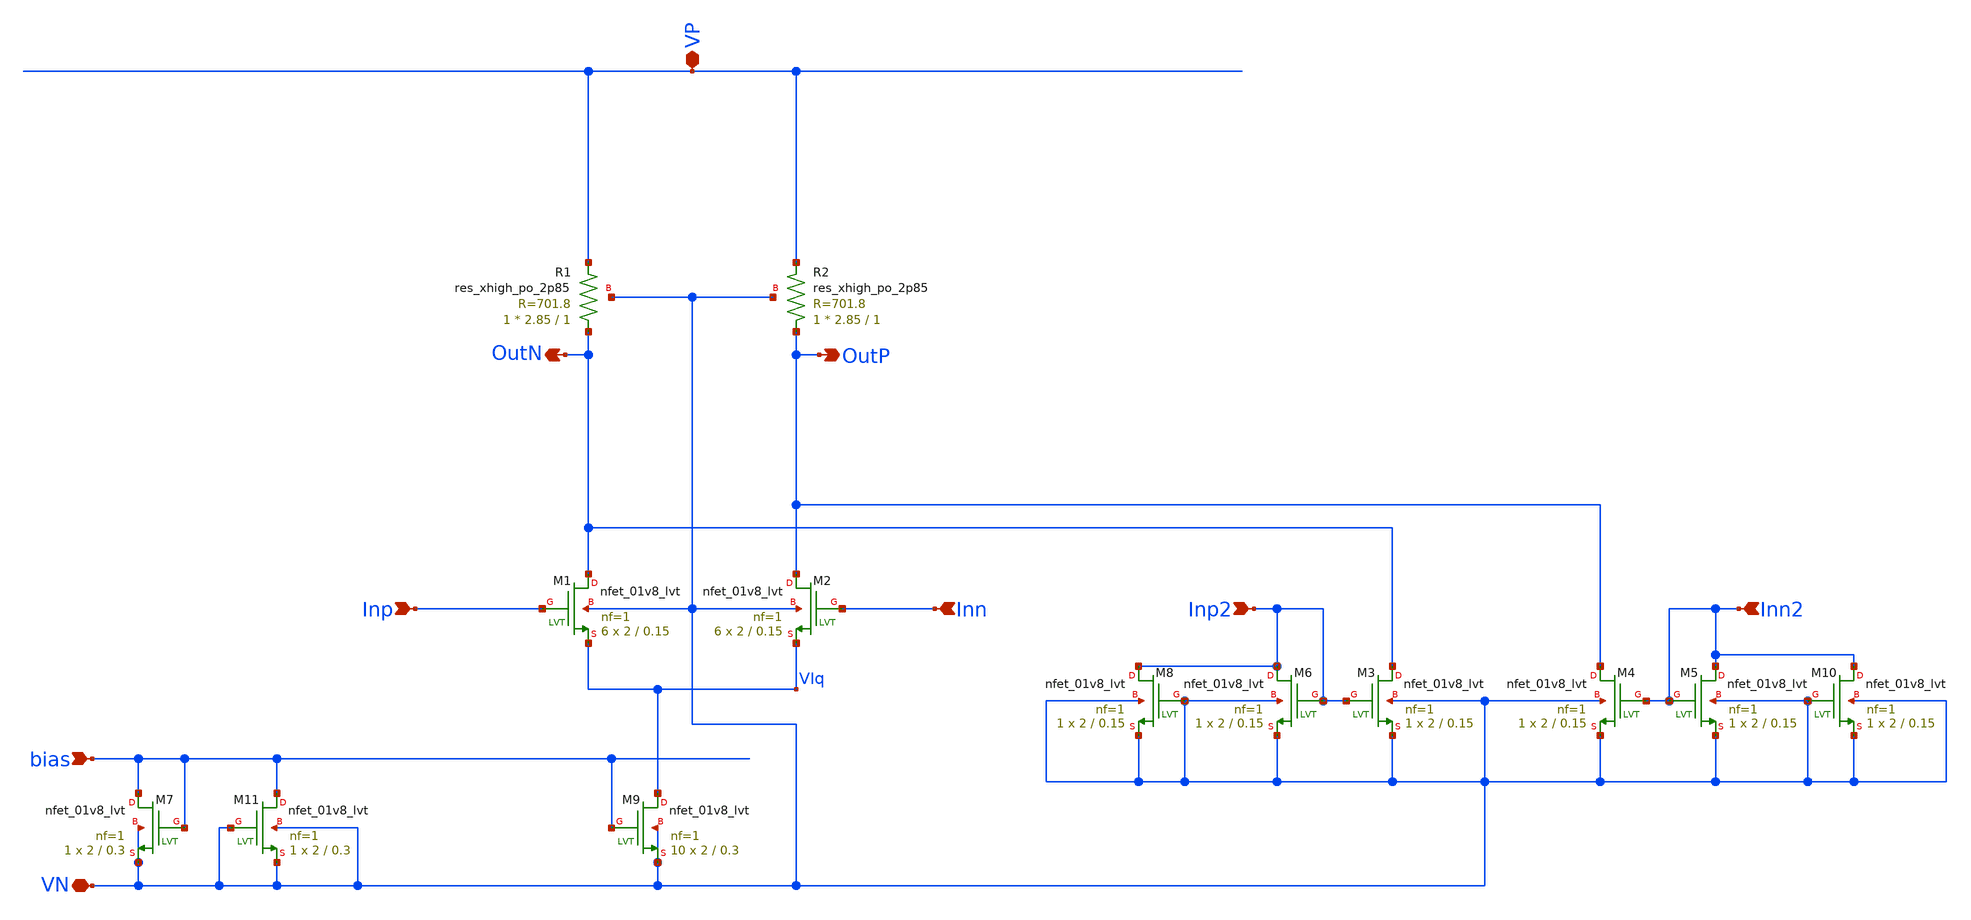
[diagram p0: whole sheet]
** sch_path: xschem/comp/comp_adv3_di.sch
**.subckt comp_adv3_di Inp bias Inn VP VN OutN OutP Inn2 Inp2
*.ipin Inp
*.ipin bias
*.ipin Inn
*.iopin VP
*.iopin VN
*.opin OutN
*.opin OutP
*.ipin Inn2
*.ipin Inp2
XM1 OutN Inp VIq VN sky130_fd_pr__nfet_01v8_lvt L=0.15 W=2 nf=1 ad='int((nf+1)/2) * W/nf * 0.29' as='int((nf+2)/2) * W/nf * 0.29'
+ pd='2*int((nf+1)/2) * (W/nf + 0.29)' ps='2*int((nf+2)/2) * (W/nf + 0.29)' nrd='0.29 / W' nrs='0.29 / W'
+ sa=0 sb=0 sd=0 mult=6 m=6
XM2 OutP Inn VIq VN sky130_fd_pr__nfet_01v8_lvt L=0.15 W=2 nf=1 ad='int((nf+1)/2) * W/nf * 0.29' as='int((nf+2)/2) * W/nf * 0.29'
+ pd='2*int((nf+1)/2) * (W/nf + 0.29)' ps='2*int((nf+2)/2) * (W/nf + 0.29)' nrd='0.29 / W' nrs='0.29 / W'
+ sa=0 sb=0 sd=0 mult=6 m=6
XM7 bias bias VN VN sky130_fd_pr__nfet_01v8_lvt L=0.3 W=2 nf=1 ad='int((nf+1)/2) * W/nf * 0.29' as='int((nf+2)/2) * W/nf * 0.29'
+ pd='2*int((nf+1)/2) * (W/nf + 0.29)' ps='2*int((nf+2)/2) * (W/nf + 0.29)' nrd='0.29 / W' nrs='0.29 / W'
+ sa=0 sb=0 sd=0 mult=1 m=1
XM9 VIq bias VN VN sky130_fd_pr__nfet_01v8_lvt L=0.3 W=2 nf=1 ad='int((nf+1)/2) * W/nf * 0.29' as='int((nf+2)/2) * W/nf * 0.29'
+ pd='2*int((nf+1)/2) * (W/nf + 0.29)' ps='2*int((nf+2)/2) * (W/nf + 0.29)' nrd='0.29 / W' nrs='0.29 / W'
+ sa=0 sb=0 sd=0 mult=10 m=10
XR1 OutN VP VN sky130_fd_pr__res_xhigh_po_2p85 L=1 mult=1 m=1
XR2 OutP VP VN sky130_fd_pr__res_xhigh_po_2p85 L=1 mult=1 m=1
XM3 OutN Inp2 VN VN sky130_fd_pr__nfet_01v8_lvt L=0.15 W=2 nf=1 ad='int((nf+1)/2) * W/nf * 0.29' as='int((nf+2)/2) * W/nf * 0.29'
+ pd='2*int((nf+1)/2) * (W/nf + 0.29)' ps='2*int((nf+2)/2) * (W/nf + 0.29)' nrd='0.29 / W' nrs='0.29 / W'
+ sa=0 sb=0 sd=0 mult=1 m=1
XM4 OutP Inn2 VN VN sky130_fd_pr__nfet_01v8_lvt L=0.15 W=2 nf=1 ad='int((nf+1)/2) * W/nf * 0.29' as='int((nf+2)/2) * W/nf * 0.29'
+ pd='2*int((nf+1)/2) * (W/nf + 0.29)' ps='2*int((nf+2)/2) * (W/nf + 0.29)' nrd='0.29 / W' nrs='0.29 / W'
+ sa=0 sb=0 sd=0 mult=1 m=1
XM5 Inn2 Inn2 VN VN sky130_fd_pr__nfet_01v8_lvt L=0.15 W=2 nf=1 ad='int((nf+1)/2) * W/nf * 0.29' as='int((nf+2)/2) * W/nf * 0.29'
+ pd='2*int((nf+1)/2) * (W/nf + 0.29)' ps='2*int((nf+2)/2) * (W/nf + 0.29)' nrd='0.29 / W' nrs='0.29 / W'
+ sa=0 sb=0 sd=0 mult=1 m=1
XM6 Inp2 Inp2 VN VN sky130_fd_pr__nfet_01v8_lvt L=0.15 W=2 nf=1 ad='int((nf+1)/2) * W/nf * 0.29' as='int((nf+2)/2) * W/nf * 0.29'
+ pd='2*int((nf+1)/2) * (W/nf + 0.29)' ps='2*int((nf+2)/2) * (W/nf + 0.29)' nrd='0.29 / W' nrs='0.29 / W'
+ sa=0 sb=0 sd=0 mult=1 m=1
XM8 Inp2 VN VN VN sky130_fd_pr__nfet_01v8_lvt L=0.15 W=2 nf=1 ad='int((nf+1)/2) * W/nf * 0.29' as='int((nf+2)/2) * W/nf * 0.29'
+ pd='2*int((nf+1)/2) * (W/nf + 0.29)' ps='2*int((nf+2)/2) * (W/nf + 0.29)' nrd='0.29 / W' nrs='0.29 / W'
+ sa=0 sb=0 sd=0 mult=1 m=1
XM10 Inn2 VN VN VN sky130_fd_pr__nfet_01v8_lvt L=0.15 W=2 nf=1 ad='int((nf+1)/2) * W/nf * 0.29' as='int((nf+2)/2) * W/nf * 0.29'
+ pd='2*int((nf+1)/2) * (W/nf + 0.29)' ps='2*int((nf+2)/2) * (W/nf + 0.29)' nrd='0.29 / W' nrs='0.29 / W'
+ sa=0 sb=0 sd=0 mult=1 m=1
XM11 bias VN VN VN sky130_fd_pr__nfet_01v8_lvt L=0.3 W=2 nf=1 ad='int((nf+1)/2) * W/nf * 0.29' as='int((nf+2)/2) * W/nf * 0.29'
+ pd='2*int((nf+1)/2) * (W/nf + 0.29)' ps='2*int((nf+2)/2) * (W/nf + 0.29)' nrd='0.29 / W' nrs='0.29 / W'
+ sa=0 sb=0 sd=0 mult=1 m=1
**** begin user architecture code

*.lib $::SKYWATER_MODELS/sky130.lib.spice tt
.lib $::SKYWATER_MODELS/sky130.lib.spice.tt.red tt



*.options savecurrents
.option warn=1
.control
set wr_vecnames
set wr_singlescale
* Power consumption
op
* save all
* #OP#
print @m.xm1.msky130_fd_pr__nfet_01v8_lvt[gds]
print vdd#branch
print v(vm2d)
print v(vm3d)
print v(UD_M5)
wrdata 'result_op.csv' vdd#branch
ac dec 10 1 10G
meas ac dc_gain_vm2d FIND vdb(vm2d) AT=1
let bw_amp_vm2d=dc_gain_vm2d-3
meas ac dc_gain_vm3d FIND vdb(vm3d) AT=1
let bw_amp_vm3d=dc_gain_vm3d-3
meas ac bw_vm2d when vdb(vm2d)=bw_amp_vm2d
meas ac bw_vm3d when vdb(vm3d)=bw_amp_vm3d
*MEAS AC phasem FIND vp(vm2d) WHEN vdb(vm2d)=0
* wrdata 'result_ac.csv' dc_gain bw
* plot vdb(vm2D) log
*
*print WM3D
run
reset
save @m.xm1.msky130_fd_pr__nfet_01v8_lvt[gds]
save @m.xm1.msky130_fd_pr__nfet_01v8_lvt[gm]
save @m.xm1.msky130_fd_pr__nfet_01v8_lvt[cgs]
save @m.xm1.msky130_fd_pr__nfet_01v8_lvt[cdg]
save @m.xm2.msky130_fd_pr__nfet_01v8_lvt[gm]
save @m.xm2.msky130_fd_pr__nfet_01v8_lvt[gds]
save @m.xm2.msky130_fd_pr__nfet_01v8_lvt[cgs]
save @m.xm2.msky130_fd_pr__nfet_01v8_lvt[cdg]
save @m.xm3.msky130_fd_pr__nfet_01v8_lvt[gm]
save @m.xm3.msky130_fd_pr__nfet_01v8_lvt[gds]
save @m.xm3.msky130_fd_pr__nfet_01v8_lvt[cgs]
save @m.xm3.msky130_fd_pr__nfet_01v8_lvt[cdg]
save @m.xm4.msky130_fd_pr__nfet_01v8_lvt[gm]
save @m.xm4.msky130_fd_pr__nfet_01v8_lvt[gds]
save @m.xm4.msky130_fd_pr__nfet_01v8_lvt[cgs]
save @m.xm4.msky130_fd_pr__nfet_01v8_lvt[cdg]
save @m.xm5.msky130_fd_pr__pfet_01v8_lvt[gm]
save @m.xm5.msky130_fd_pr__pfet_01v8_lvt[gds]
save @m.xm5.msky130_fd_pr__pfet_01v8_lvt[cgs]
save @m.xm5.msky130_fd_pr__pfet_01v8_lvt[cdg]
save @m.xm6.msky130_fd_pr__pfet_01v8_lvt[gm]
save @m.xm6.msky130_fd_pr__pfet_01v8_lvt[gds]
save @m.xm6.msky130_fd_pr__pfet_01v8_lvt[cgs]
save @m.xm6.msky130_fd_pr__pfet_01v8_lvt[cdg]
save @m.xm7.msky130_fd_pr__nfet_01v8_lvt[gm]
save @m.xm7.msky130_fd_pr__nfet_01v8_lvt[gds]
save @m.xm7.msky130_fd_pr__nfet_01v8_lvt[cgs]
save @m.xm7.msky130_fd_pr__nfet_01v8_lvt[cdg]
save @m.xm8.msky130_fd_pr__nfet_01v8_lvt[gm]
save @m.xm8.msky130_fd_pr__nfet_01v8_lvt[gds]
save @m.xm8.msky130_fd_pr__nfet_01v8_lvt[cgs]
save @m.xm8.msky130_fd_pr__nfet_01v8_lvt[cdg]
save @m.xm9.msky130_fd_pr__nfet_01v8_lvt[gm]
save @m.xm9.msky130_fd_pr__nfet_01v8_lvt[gds]
save @m.xm9.msky130_fd_pr__nfet_01v8_lvt[cgs]
save @m.xm9.msky130_fd_pr__nfet_01v8_lvt[cdg]
save v(Voutp)
save v(Voutn)
save v(VIa)
save v(VIq)

save v(Vinn)
save v(Vinp)
save v(VM8G)

op
write comp.raw
run
*reset
*noise v(vm1d) I1 dec 100 1 10G
*print all
*setplot noise2
*write noise2.raw
*run
reset
ac dec 10 1 1T
plot vdb(Voutp) vdb(Voutn)
plot phase(Voutp)/pi*180 phase(Voutn)/pi*180
run
reset
tran 1ps 10ns
plot v(Vinp) v(Voutn) v(Voutp)
run
.endc


**** end user architecture code
**.ends
.end
